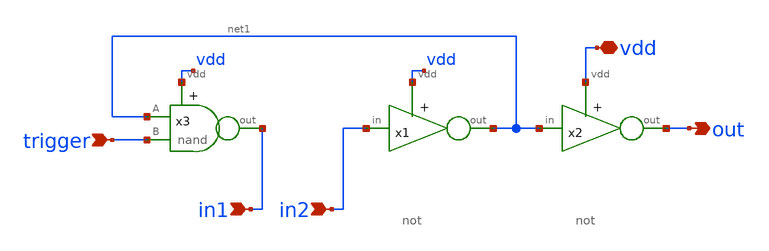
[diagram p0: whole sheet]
** sch_path: designs/subcells/core_monostable/monostable.sch
**.subckt monostable vdd trigger in1 in2 out
*.iopin vdd
*.ipin trigger
*.ipin in1
*.ipin in2
*.opin out
x1 vdd in2 net1 not
x2 vdd net1 out not
x3 vdd in1 net1 trigger nand
**.ends

* expanding   symbol:  /foss/designs/spike_130/designs/subcells/core_not/not.sym # of pins=3
** sym_path: designs/subcells/core_not/not.sym
** sch_path: designs/subcells/core_not/not.sch
.subckt not vdd in out
*.ipin in
*.opin out
*.iopin vdd
XM10 out in vdd vdd sky130_fd_pr__pfet_01v8_lvt L=0.35 W=1 nf=1 ad='int((1 + 1)/2) * 1 / 1 * 0.29' as='int((1 + 2)/2) * 1 / 1 * 0.29'
+ pd='2*int((1 + 1)/2) * (1 / 1 + 0.29)' ps='2*int((1 + 2)/2) * (1 / 1 + 0.29)' nrd='0.29 / 1 ' nrs='0.29 / 1 '
+ sa=0 sb=0 sd=0 mult=1 m=1
XM1 out in GND GND sky130_fd_pr__nfet_01v8_lvt L=0.15 W=1 nf=1 ad='int((1 + 1)/2) * 1 / 1 * 0.29' as='int((1 + 2)/2) * 1 / 1 * 0.29'
+ pd='2*int((1 + 1)/2) * (1 / 1 + 0.29)' ps='2*int((1 + 2)/2) * (1 / 1 + 0.29)' nrd='0.29 / 1 ' nrs='0.29 / 1 '
+ sa=0 sb=0 sd=0 mult=1 m=1
.ends


* expanding   symbol:  /foss/designs/spike_130/designs/subcells/core_nand/nand.sym # of pins=4
** sym_path: designs/subcells/core_nand/nand.sym
** sch_path: designs/subcells/core_nand/nand.sch
.subckt nand vdd out A B
*.iopin vdd
*.opin out
*.ipin A
*.ipin B
XM4 net1 B GND GND sky130_fd_pr__nfet_01v8_lvt L=0.15 W=1 nf=1 ad='int((1 + 1)/2) * 1 / 1 * 0.29' as='int((1 + 2)/2) * 1 / 1 * 0.29'
+ pd='2*int((1 + 1)/2) * (1 / 1 + 0.29)' ps='2*int((1 + 2)/2) * (1 / 1 + 0.29)' nrd='0.29 / 1 ' nrs='0.29 / 1 '
+ sa=0 sb=0 sd=0 mult=1 m=1
XM1 out B vdd vdd sky130_fd_pr__pfet_01v8_lvt L=0.35 W=1 nf=1 ad='int((1 + 1)/2) * 1 / 1 * 0.29' as='int((1 + 2)/2) * 1 / 1 * 0.29'
+ pd='2*int((1 + 1)/2) * (1 / 1 + 0.29)' ps='2*int((1 + 2)/2) * (1 / 1 + 0.29)' nrd='0.29 / 1 ' nrs='0.29 / 1 '
+ sa=0 sb=0 sd=0 mult=1 m=1
XM2 out A vdd vdd sky130_fd_pr__pfet_01v8_lvt L=0.35 W=1 nf=1 ad='int((1 + 1)/2) * 1 / 1 * 0.29' as='int((1 + 2)/2) * 1 / 1 * 0.29'
+ pd='2*int((1 + 1)/2) * (1 / 1 + 0.29)' ps='2*int((1 + 2)/2) * (1 / 1 + 0.29)' nrd='0.29 / 1 ' nrs='0.29 / 1 '
+ sa=0 sb=0 sd=0 mult=1 m=1
XM3 out A net1 GND sky130_fd_pr__nfet_01v8_lvt L=0.15 W=1 nf=1 ad='int((1 + 1)/2) * 1 / 1 * 0.29' as='int((1 + 2)/2) * 1 / 1 * 0.29'
+ pd='2*int((1 + 1)/2) * (1 / 1 + 0.29)' ps='2*int((1 + 2)/2) * (1 / 1 + 0.29)' nrd='0.29 / 1 ' nrs='0.29 / 1 '
+ sa=0 sb=0 sd=0 mult=1 m=1
.ends

.GLOBAL GND
.end
